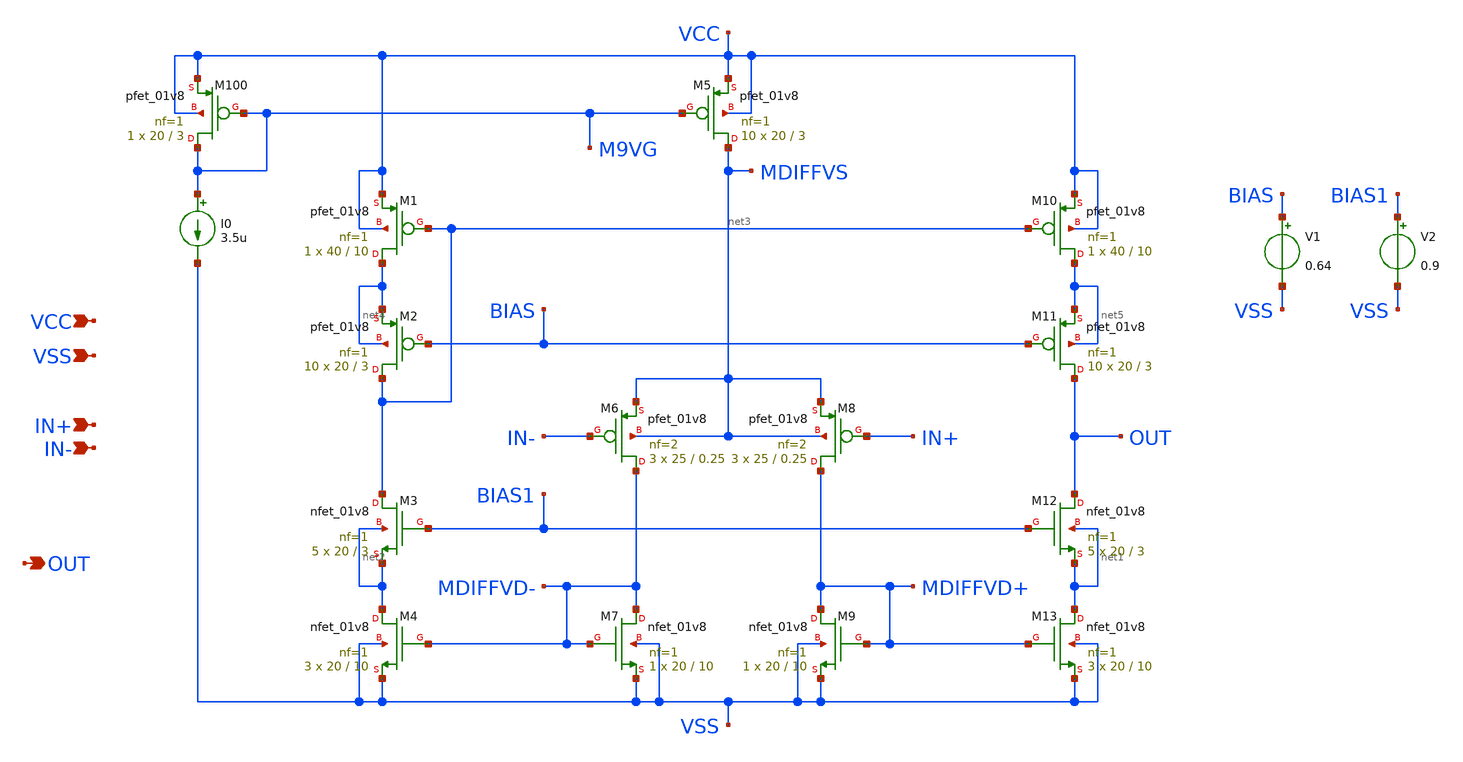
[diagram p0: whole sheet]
** sch_path: opamp_cascode.sch
**.subckt opamp_cascode IN+ IN- VCC VSS OUT
*.ipin IN+
*.ipin IN-
*.ipin VCC
*.ipin VSS
*.opin OUT
XM10 net5 net3 VCC VCC sky130_fd_pr__pfet_01v8 L=10 W=40 nf=1 ad='int((nf+1)/2) * W/nf * 0.29' as='int((nf+2)/2) * W/nf * 0.29'
+ pd='2*int((nf+1)/2) * (W/nf + 0.29)' ps='2*int((nf+2)/2) * (W/nf + 0.29)' nrd='0.29 / W' nrs='0.29 / W'
+ sa=0 sb=0 sd=0 mult=1 m=1
XM1 net4 net3 VCC VCC sky130_fd_pr__pfet_01v8 L=10 W=40 nf=1 ad='int((nf+1)/2) * W/nf * 0.29' as='int((nf+2)/2) * W/nf * 0.29'
+ pd='2*int((nf+1)/2) * (W/nf + 0.29)' ps='2*int((nf+2)/2) * (W/nf + 0.29)' nrd='0.29 / W' nrs='0.29 / W'
+ sa=0 sb=0 sd=0 mult=1 m=1
XM5 MDIFFVS M9VG VCC VCC sky130_fd_pr__pfet_01v8 L=3 W=20 nf=1 ad='int((nf+1)/2) * W/nf * 0.29' as='int((nf+2)/2) * W/nf * 0.29'
+ pd='2*int((nf+1)/2) * (W/nf + 0.29)' ps='2*int((nf+2)/2) * (W/nf + 0.29)' nrd='0.29 / W' nrs='0.29 / W'
+ sa=0 sb=0 sd=0 mult=10 m=10
XM100 M9VG M9VG VCC VCC sky130_fd_pr__pfet_01v8 L=3 W=20 nf=1 ad='int((nf+1)/2) * W/nf * 0.29' as='int((nf+2)/2) * W/nf * 0.29'
+ pd='2*int((nf+1)/2) * (W/nf + 0.29)' ps='2*int((nf+2)/2) * (W/nf + 0.29)' nrd='0.29 / W' nrs='0.29 / W'
+ sa=0 sb=0 sd=0 mult=1 m=1
I0 M9VG VSS 3.5u
XM11 OUT BIAS net5 net5 sky130_fd_pr__pfet_01v8 L=3 W=20 nf=1 ad='int((nf+1)/2) * W/nf * 0.29' as='int((nf+2)/2) * W/nf * 0.29'
+ pd='2*int((nf+1)/2) * (W/nf + 0.29)' ps='2*int((nf+2)/2) * (W/nf + 0.29)' nrd='0.29 / W' nrs='0.29 / W'
+ sa=0 sb=0 sd=0 mult=10 m=10
XM2 net3 BIAS net4 net4 sky130_fd_pr__pfet_01v8 L=3 W=20 nf=1 ad='int((nf+1)/2) * W/nf * 0.29' as='int((nf+2)/2) * W/nf * 0.29'
+ pd='2*int((nf+1)/2) * (W/nf + 0.29)' ps='2*int((nf+2)/2) * (W/nf + 0.29)' nrd='0.29 / W' nrs='0.29 / W'
+ sa=0 sb=0 sd=0 mult=10 m=10
XM6 MDIFFVD- IN- MDIFFVS MDIFFVS sky130_fd_pr__pfet_01v8 L=0.25 W=25 nf=2 ad='int((nf+1)/2) * W/nf * 0.29'
+ as='int((nf+2)/2) * W/nf * 0.29' pd='2*int((nf+1)/2) * (W/nf + 0.29)' ps='2*int((nf+2)/2) * (W/nf + 0.29)'
+ nrd='0.29 / W' nrs='0.29 / W' sa=0 sb=0 sd=0 mult=3 m=3
XM8 MDIFFVD+ IN+ MDIFFVS MDIFFVS sky130_fd_pr__pfet_01v8 L=0.25 W=25 nf=2 ad='int((nf+1)/2) * W/nf * 0.29'
+ as='int((nf+2)/2) * W/nf * 0.29' pd='2*int((nf+1)/2) * (W/nf + 0.29)' ps='2*int((nf+2)/2) * (W/nf + 0.29)'
+ nrd='0.29 / W' nrs='0.29 / W' sa=0 sb=0 sd=0 mult=3 m=3
XM7 MDIFFVD- MDIFFVD- VSS VSS sky130_fd_pr__nfet_01v8 L=10 W=20 nf=1 ad='int((nf+1)/2) * W/nf * 0.29'
+ as='int((nf+2)/2) * W/nf * 0.29' pd='2*int((nf+1)/2) * (W/nf + 0.29)' ps='2*int((nf+2)/2) * (W/nf + 0.29)'
+ nrd='0.29 / W' nrs='0.29 / W' sa=0 sb=0 sd=0 mult=1 m=1
XM9 MDIFFVD+ MDIFFVD+ VSS VSS sky130_fd_pr__nfet_01v8 L=10 W=20 nf=1 ad='int((nf+1)/2) * W/nf * 0.29'
+ as='int((nf+2)/2) * W/nf * 0.29' pd='2*int((nf+1)/2) * (W/nf + 0.29)' ps='2*int((nf+2)/2) * (W/nf + 0.29)'
+ nrd='0.29 / W' nrs='0.29 / W' sa=0 sb=0 sd=0 mult=1 m=1
XM13 net1 MDIFFVD+ VSS VSS sky130_fd_pr__nfet_01v8 L=10 W=20 nf=1 ad='int((nf+1)/2) * W/nf * 0.29' as='int((nf+2)/2) * W/nf * 0.29'
+ pd='2*int((nf+1)/2) * (W/nf + 0.29)' ps='2*int((nf+2)/2) * (W/nf + 0.29)' nrd='0.29 / W' nrs='0.29 / W'
+ sa=0 sb=0 sd=0 mult=3 m=3
XM4 net2 MDIFFVD- VSS VSS sky130_fd_pr__nfet_01v8 L=10 W=20 nf=1 ad='int((nf+1)/2) * W/nf * 0.29' as='int((nf+2)/2) * W/nf * 0.29'
+ pd='2*int((nf+1)/2) * (W/nf + 0.29)' ps='2*int((nf+2)/2) * (W/nf + 0.29)' nrd='0.29 / W' nrs='0.29 / W'
+ sa=0 sb=0 sd=0 mult=3 m=3
XM12 OUT BIAS1 net1 net1 sky130_fd_pr__nfet_01v8 L=3 W=20 nf=1 ad='int((nf+1)/2) * W/nf * 0.29' as='int((nf+2)/2) * W/nf * 0.29'
+ pd='2*int((nf+1)/2) * (W/nf + 0.29)' ps='2*int((nf+2)/2) * (W/nf + 0.29)' nrd='0.29 / W' nrs='0.29 / W'
+ sa=0 sb=0 sd=0 mult=5 m=5
XM3 net3 BIAS1 net2 net2 sky130_fd_pr__nfet_01v8 L=3 W=20 nf=1 ad='int((nf+1)/2) * W/nf * 0.29' as='int((nf+2)/2) * W/nf * 0.29'
+ pd='2*int((nf+1)/2) * (W/nf + 0.29)' ps='2*int((nf+2)/2) * (W/nf + 0.29)' nrd='0.29 / W' nrs='0.29 / W'
+ sa=0 sb=0 sd=0 mult=5 m=5
V1 BIAS VSS 0.64
V2 BIAS1 VSS 0.9
**.ends
.end
